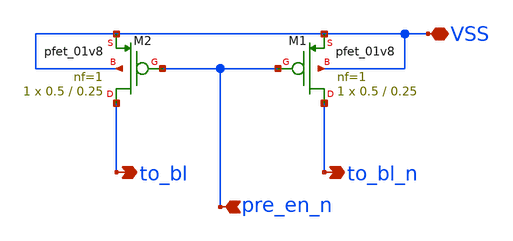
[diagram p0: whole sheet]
** sch_path: precharge.sch
**.subckt precharge pre_en_n to_bl to_bl_n VSS
*.ipin pre_en_n
*.opin to_bl
*.opin to_bl_n
*.iopin VSS
XM1 to_bl_n pre_en_n VSS VSS sky130_fd_pr__pfet_01v8 L=0.25 W=0.5 nf=1 ad='int((nf+1)/2) * W/nf * 0.29'
+ as='int((nf+2)/2) * W/nf * 0.29' pd='2*int((nf+1)/2) * (W/nf + 0.29)' ps='2*int((nf+2)/2) * (W/nf + 0.29)'
+ nrd='0.29 / W' nrs='0.29 / W' sa=0 sb=0 sd=0 mult=1 m=1
XM2 to_bl pre_en_n VSS VSS sky130_fd_pr__pfet_01v8 L=0.25 W=0.5 nf=1 ad='int((nf+1)/2) * W/nf * 0.29'
+ as='int((nf+2)/2) * W/nf * 0.29' pd='2*int((nf+1)/2) * (W/nf + 0.29)' ps='2*int((nf+2)/2) * (W/nf + 0.29)'
+ nrd='0.29 / W' nrs='0.29 / W' sa=0 sb=0 sd=0 mult=1 m=1
**.ends
.end
